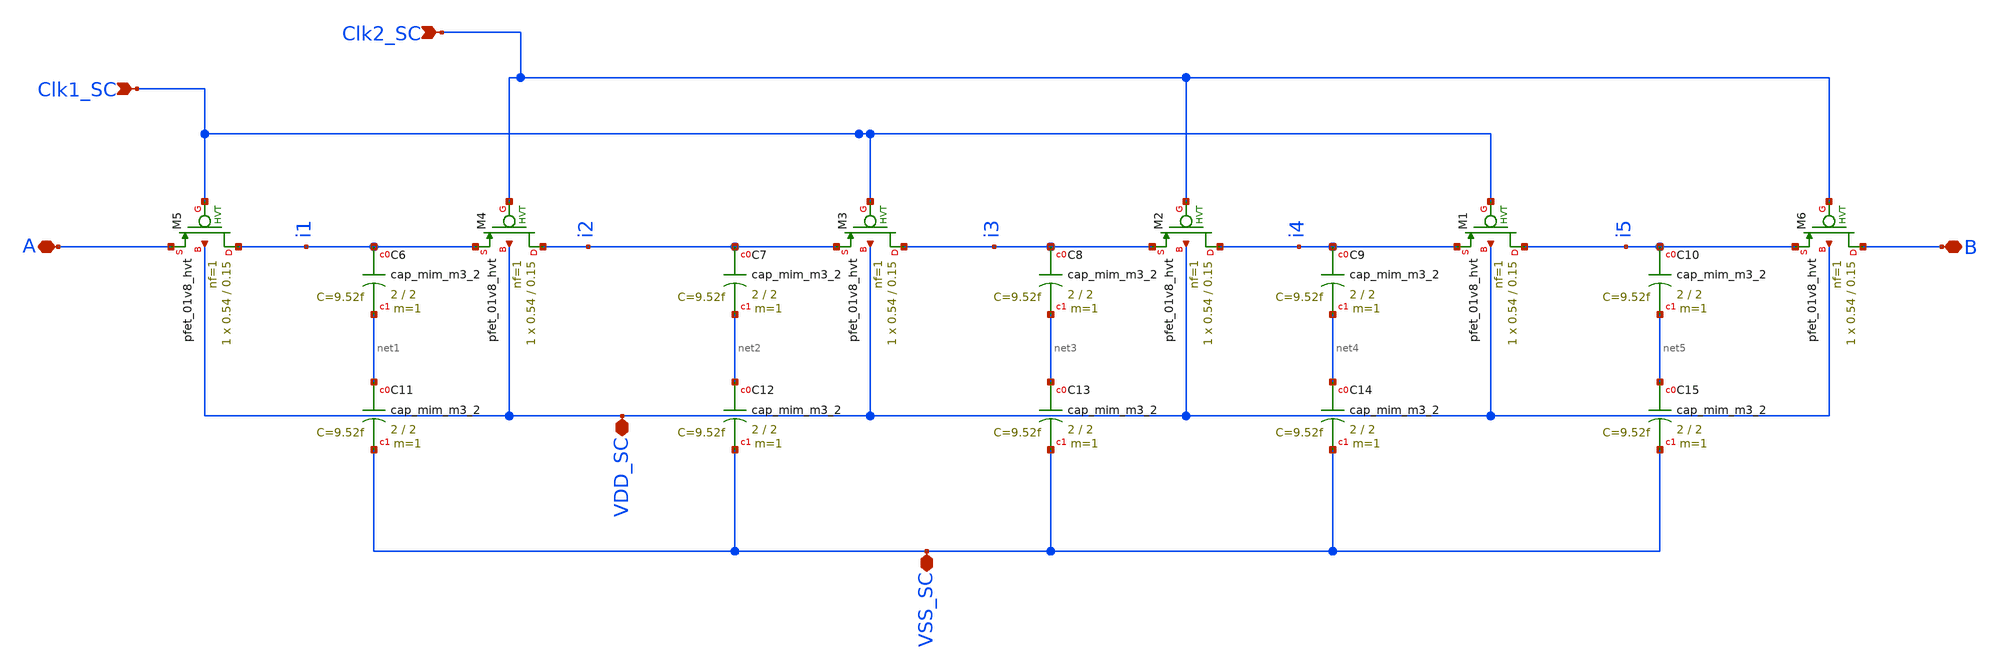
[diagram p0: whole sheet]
** sch_path: lna_res_sc.sch
**.subckt lna_res_sc A Clk1_SC Clk2_SC VSS_SC B VDD_SC
*.iopin A
*.ipin Clk1_SC
*.ipin Clk2_SC
*.iopin VSS_SC
*.iopin B
*.iopin VDD_SC
XM1 i5 Clk1_SC i4 VDD_SC sky130_fd_pr__pfet_01v8_hvt L=0.15 W=0.54 nf=1 ad='int((nf+1)/2) * W/nf * 0.29'
+ as='int((nf+2)/2) * W/nf * 0.29' pd='2*int((nf+1)/2) * (W/nf + 0.29)' ps='2*int((nf+2)/2) * (W/nf + 0.29)'
+ nrd='0.29 / W' nrs='0.29 / W' sa=0 sb=0 sd=0 mult=1 m=1
XM2 i4 Clk2_SC i3 VDD_SC sky130_fd_pr__pfet_01v8_hvt L=0.15 W=0.54 nf=1 ad='int((nf+1)/2) * W/nf * 0.29'
+ as='int((nf+2)/2) * W/nf * 0.29' pd='2*int((nf+1)/2) * (W/nf + 0.29)' ps='2*int((nf+2)/2) * (W/nf + 0.29)'
+ nrd='0.29 / W' nrs='0.29 / W' sa=0 sb=0 sd=0 mult=1 m=1
XM3 i3 Clk1_SC i2 VDD_SC sky130_fd_pr__pfet_01v8_hvt L=0.15 W=0.54 nf=1 ad='int((nf+1)/2) * W/nf * 0.29'
+ as='int((nf+2)/2) * W/nf * 0.29' pd='2*int((nf+1)/2) * (W/nf + 0.29)' ps='2*int((nf+2)/2) * (W/nf + 0.29)'
+ nrd='0.29 / W' nrs='0.29 / W' sa=0 sb=0 sd=0 mult=1 m=1
XM4 i2 Clk2_SC i1 VDD_SC sky130_fd_pr__pfet_01v8_hvt L=0.15 W=0.54 nf=1 ad='int((nf+1)/2) * W/nf * 0.29'
+ as='int((nf+2)/2) * W/nf * 0.29' pd='2*int((nf+1)/2) * (W/nf + 0.29)' ps='2*int((nf+2)/2) * (W/nf + 0.29)'
+ nrd='0.29 / W' nrs='0.29 / W' sa=0 sb=0 sd=0 mult=1 m=1
XM5 i1 Clk1_SC A VDD_SC sky130_fd_pr__pfet_01v8_hvt L=0.15 W=0.54 nf=1 ad='int((nf+1)/2) * W/nf * 0.29'
+ as='int((nf+2)/2) * W/nf * 0.29' pd='2*int((nf+1)/2) * (W/nf + 0.29)' ps='2*int((nf+2)/2) * (W/nf + 0.29)'
+ nrd='0.29 / W' nrs='0.29 / W' sa=0 sb=0 sd=0 mult=1 m=1
XM6 B Clk2_SC i5 VDD_SC sky130_fd_pr__pfet_01v8_hvt L=0.15 W=0.54 nf=1 ad='int((nf+1)/2) * W/nf * 0.29'
+ as='int((nf+2)/2) * W/nf * 0.29' pd='2*int((nf+1)/2) * (W/nf + 0.29)' ps='2*int((nf+2)/2) * (W/nf + 0.29)'
+ nrd='0.29 / W' nrs='0.29 / W' sa=0 sb=0 sd=0 mult=1 m=1
XC6 i1 net1 sky130_fd_pr__cap_mim_m3_2 W=2 L=2 MF=1 m=1
XC7 i2 net2 sky130_fd_pr__cap_mim_m3_2 W=2 L=2 MF=1 m=1
XC8 i3 net3 sky130_fd_pr__cap_mim_m3_2 W=2 L=2 MF=1 m=1
XC9 i4 net4 sky130_fd_pr__cap_mim_m3_2 W=2 L=2 MF=1 m=1
XC10 i5 net5 sky130_fd_pr__cap_mim_m3_2 W=2 L=2 MF=1 m=1
XC11 net1 VSS_SC sky130_fd_pr__cap_mim_m3_2 W=2 L=2 MF=1 m=1
XC12 net2 VSS_SC sky130_fd_pr__cap_mim_m3_2 W=2 L=2 MF=1 m=1
XC13 net3 VSS_SC sky130_fd_pr__cap_mim_m3_2 W=2 L=2 MF=1 m=1
XC14 net4 VSS_SC sky130_fd_pr__cap_mim_m3_2 W=2 L=2 MF=1 m=1
XC15 net5 VSS_SC sky130_fd_pr__cap_mim_m3_2 W=2 L=2 MF=1 m=1
**.ends
.end
